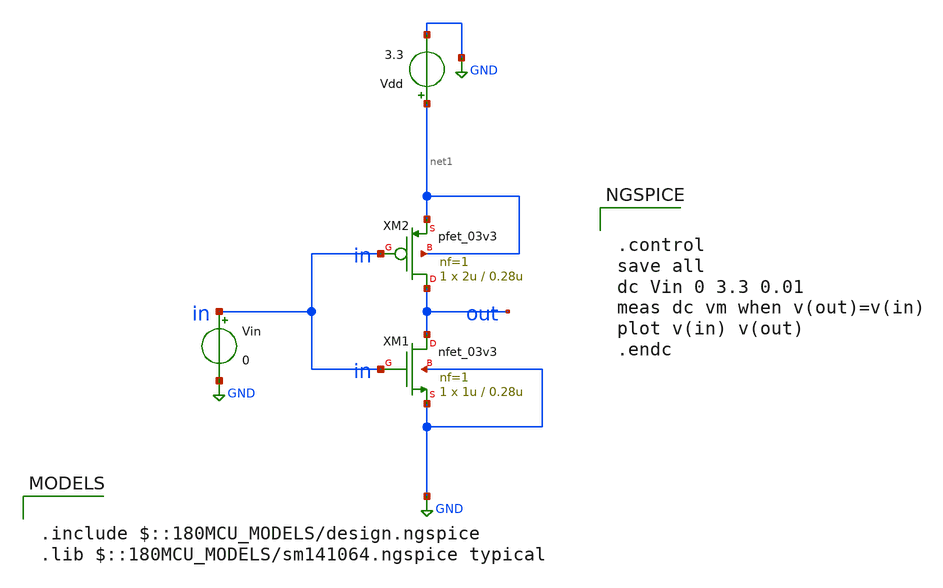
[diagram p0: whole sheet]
** sch_path: xschem/pll_dac/inverter.sch
**.subckt inverter
XM1 out in GND GND nfet_03v3 L=0.28u W=1u nf=1 ad='int((nf+1)/2) * W/nf * 0.18u' as='int((nf+2)/2) * W/nf * 0.18u'
+ pd='2*int((nf+1)/2) * (W/nf + 0.18u)' ps='2*int((nf+2)/2) * (W/nf + 0.18u)' nrd='0.18u / W' nrs='0.18u / W'
+ sa=0 sb=0 sd=0 m=1
XM2 out in net1 net1 pfet_03v3 L=0.28u W=2u nf=1 ad='int((nf+1)/2) * W/nf * 0.18u' as='int((nf+2)/2) * W/nf * 0.18u'
+ pd='2*int((nf+1)/2) * (W/nf + 0.18u)' ps='2*int((nf+2)/2) * (W/nf + 0.18u)' nrd='0.18u / W' nrs='0.18u / W'
+ sa=0 sb=0 sd=0 m=1
Vdd net1 GND 3.3
Vin in GND 0
**** begin user architecture code


.control
save all
dc Vin 0 3.3 0.01
meas dc vm when v(out)=v(in)
plot v(in) v(out)
.endc



.include $::180MCU_MODELS/design.ngspice
.lib $::180MCU_MODELS/sm141064.ngspice typical

**** end user architecture code
**.ends
.GLOBAL GND
.end
